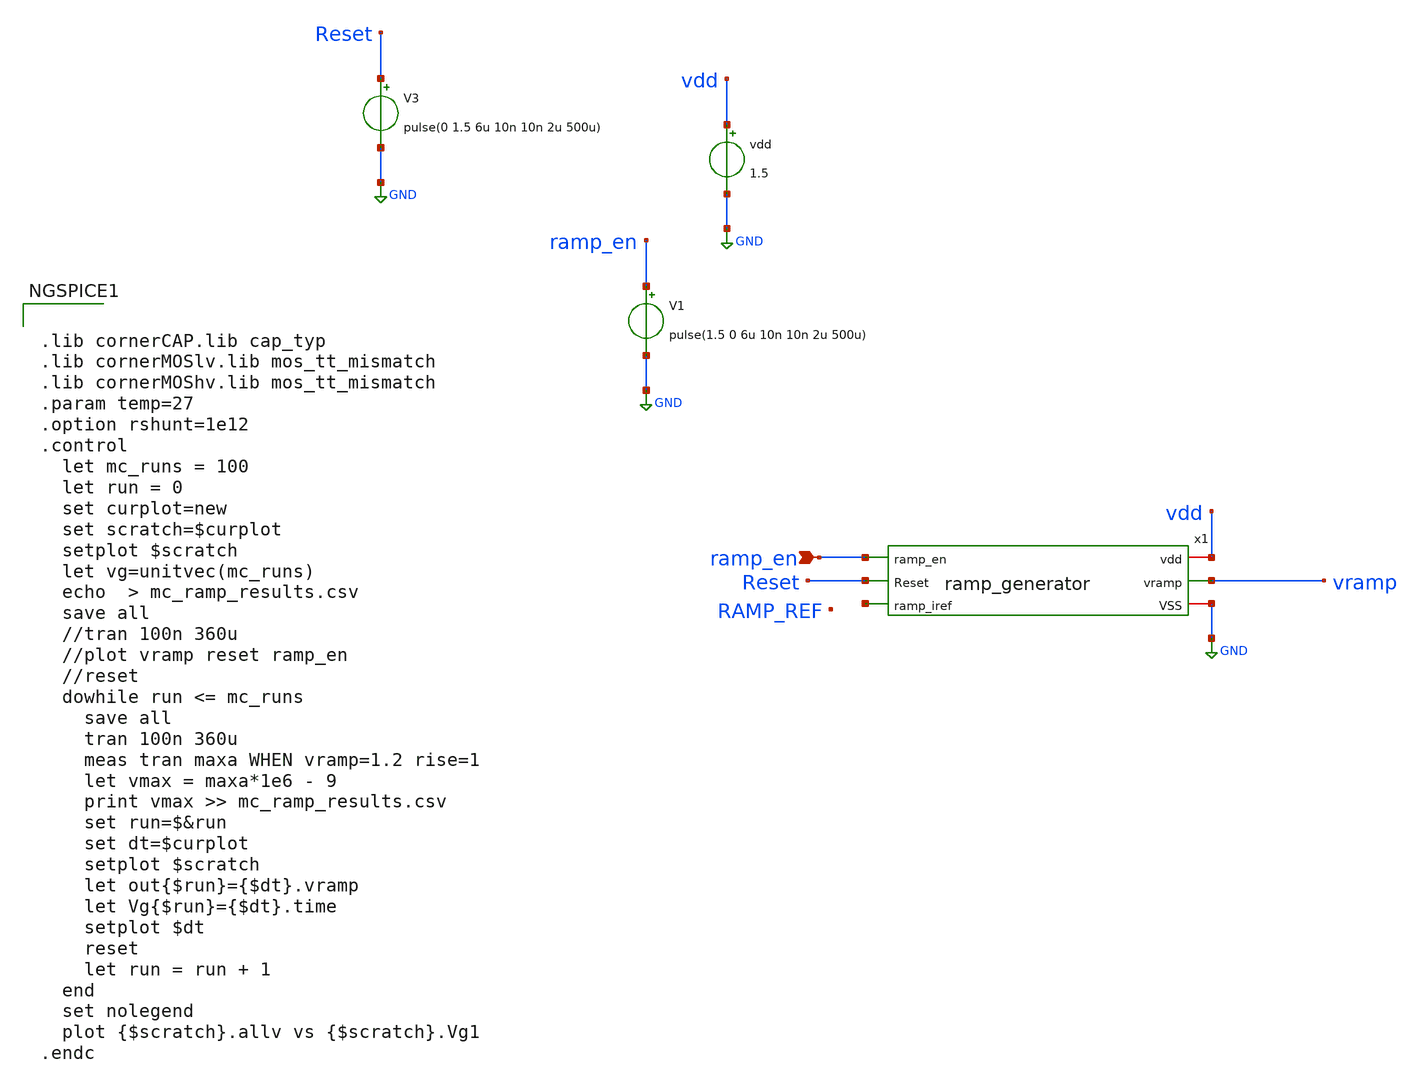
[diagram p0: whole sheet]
** sch_path: dependencies/ADC/dependencies/RAMP_GEN/RAMP_GEN-main/testbenches/corners/xschem/ramp_generator_mc.sch
**.subckt ramp_generator_mc ramp_en
*.ipin ramp_en
vdd vdd GND 1.5
V3 Reset GND pulse(0 1.5 6u 10n 10n 2u 500u)
x1 vdd ramp_en vramp Reset GND net1 Nbulk Pbulk ramp_generator
V1 ramp_en GND pulse(1.5 0 6u 10n 10n 2u 500u)
**** begin user architecture code


.lib cornerCAP.lib cap_typ
.lib cornerMOSlv.lib mos_tt_mismatch
.lib cornerMOShv.lib mos_tt_mismatch
.param temp=27
.option rshunt=1e12
.control
  let mc_runs = 100
  let run = 0
  set curplot=new
  set scratch=$curplot
  setplot $scratch
  let vg=unitvec(mc_runs)
  echo  > mc_ramp_results.csv
  save all
  //tran 100n 360u
  //plot vramp reset ramp_en
  //reset
  dowhile run <= mc_runs
    save all
    tran 100n 360u
    meas tran maxa WHEN vramp=1.2 rise=1
    let vmax = maxa*1e6 - 9
    print vmax >> mc_ramp_results.csv
    set run=$&run
    set dt=$curplot
    setplot $scratch
    let out{$run}={$dt}.vramp
    let Vg{$run}={$dt}.time
    setplot $dt
    reset
    let run = run + 1
  end
  set nolegend
  plot {$scratch}.allv vs {$scratch}.Vg1
.endc



**** end user architecture code
**.ends
.GLOBAL GND
.end
